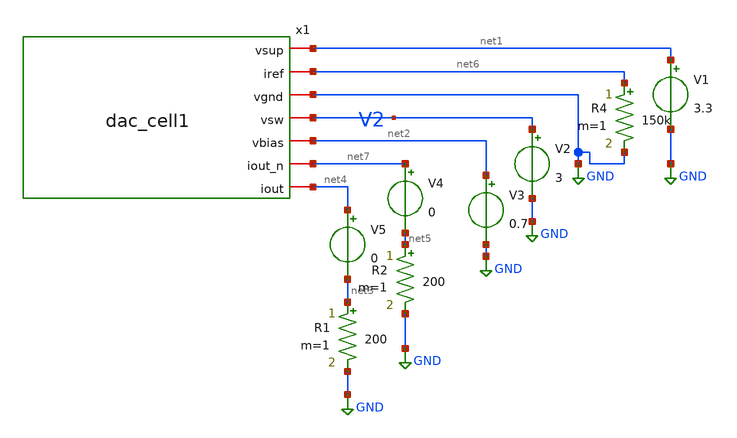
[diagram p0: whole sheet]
** sch_path: dev/dac_cell1/tb/tb_dac_cell1_op.sch
**.subckt tb_dac_cell1_op
V1 net1 GND 3.3
V2 V2 GND 3
V3 net2 GND 0.7
V4 net7 net5 0
V5 net4 net3 0
R1 net3 GND 200 m=1
R2 net5 GND 200 m=1
R4 net6 GND 150k m=1
x1 net1 net6 GND V2 net2 net7 net4 dac_cell1
**** begin user architecture code


.lib "/usr/share/pdk/sky130A/libs.tech/ngspice/sky130.lib.spice" tt
.param mc_mm_switch=0
.param mc_pr_switch=0
*** ANALYSIS TO DO

.op
.save V2 @m.x1.xm1.msky130_fd_pr__pfet_g5v0d10v5[id] @m.x1.xm2.msky130_fd_pr__pfet_g5v0d10v5[id] @m.x1.xm3.msky130_fd_pr__pfet_g5v0d10v5[id] @m.x1.xm4.msky130_fd_pr__pfet_g5v0d10v5[id]


.control
set wr_vecnames
set wr_singlescale

run
******** results filename  ************ nodes to write
wrdata $DEV_PATH/res/dac_cell1_op.res V2 @m.x1.xm1.msky130_fd_pr__pfet_g5v0d10v5[id]
+ @m.x1.xm2.msky130_fd_pr__pfet_g5v0d10v5[id] @m.x1.xm3.msky130_fd_pr__pfet_g5v0d10v5[id] @m.x1.xm4.msky130_fd_pr__pfet_g5v0d10v5[id]
.endc


**** end user architecture code
**.ends
.GLOBAL GND
.end
